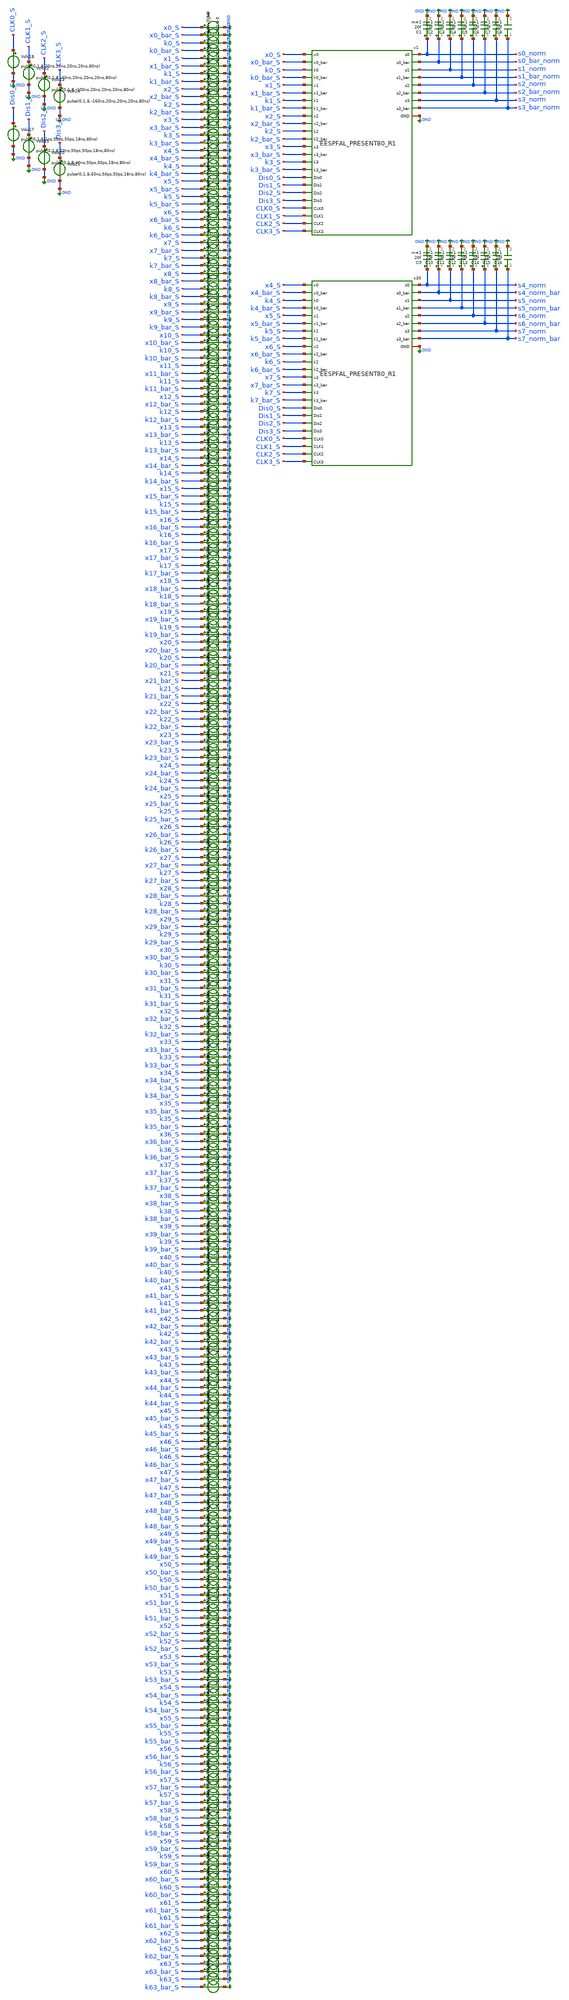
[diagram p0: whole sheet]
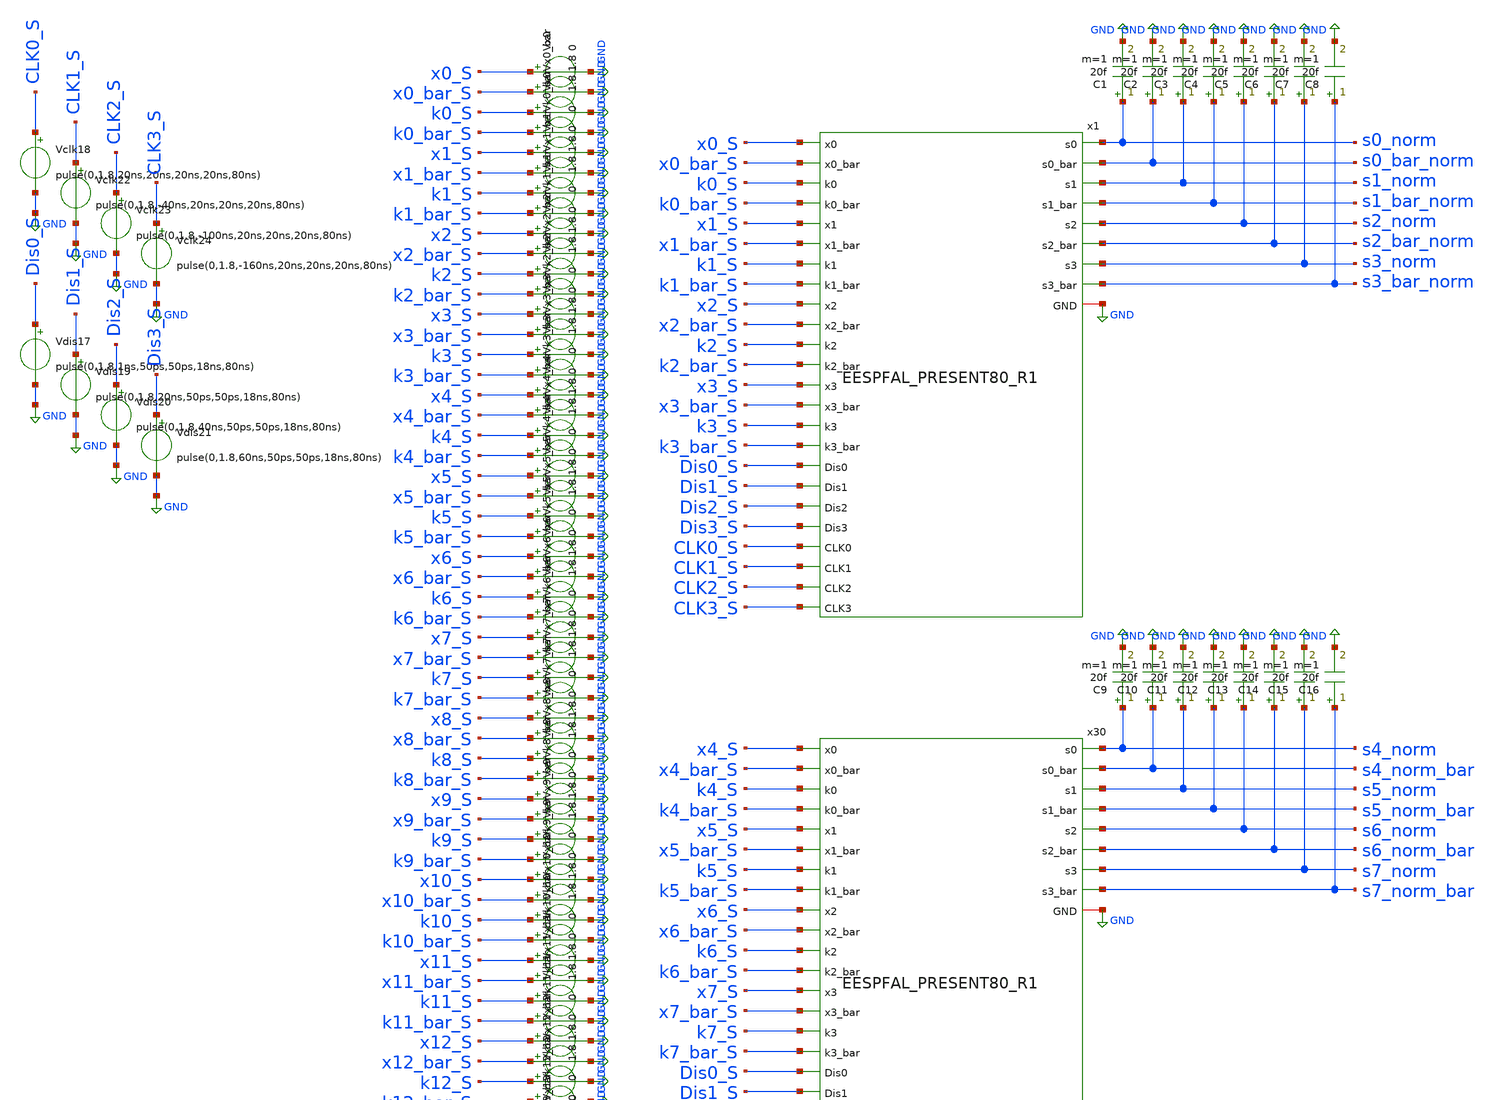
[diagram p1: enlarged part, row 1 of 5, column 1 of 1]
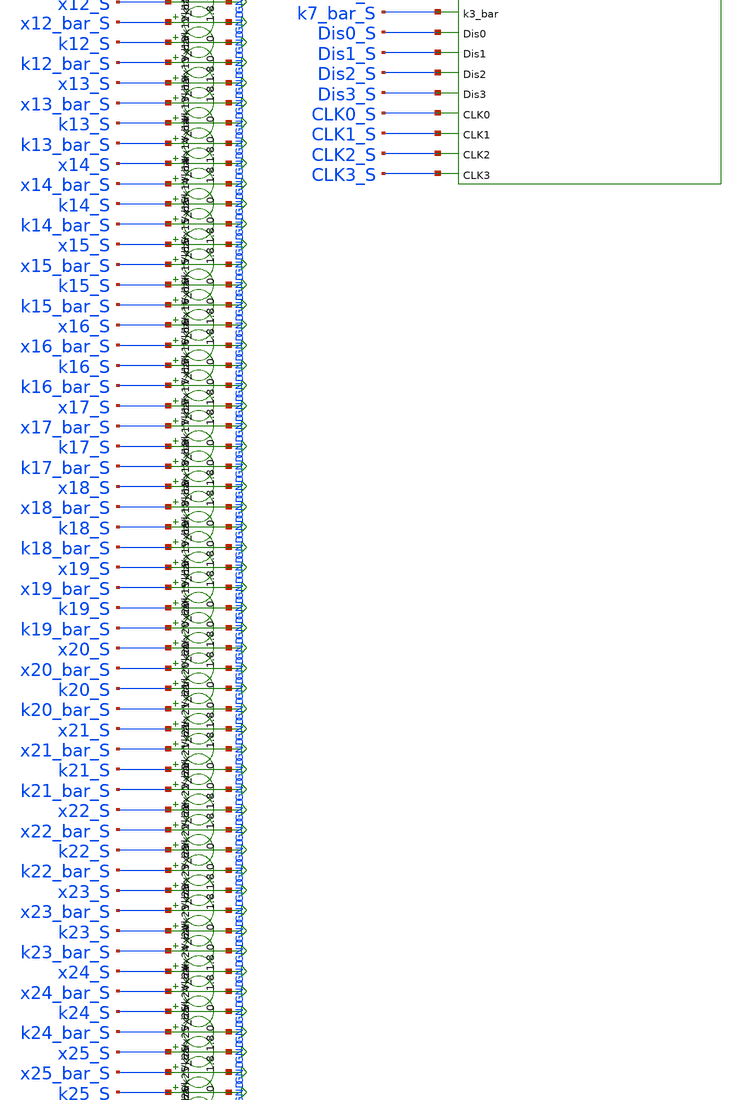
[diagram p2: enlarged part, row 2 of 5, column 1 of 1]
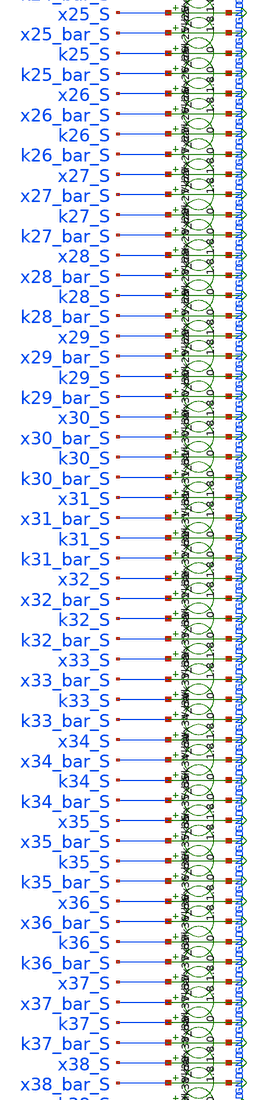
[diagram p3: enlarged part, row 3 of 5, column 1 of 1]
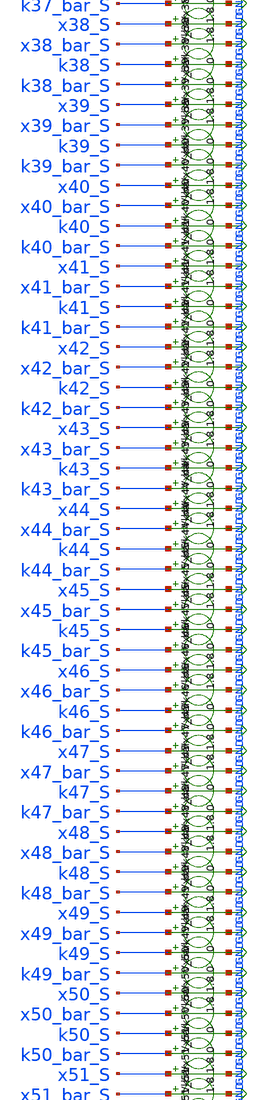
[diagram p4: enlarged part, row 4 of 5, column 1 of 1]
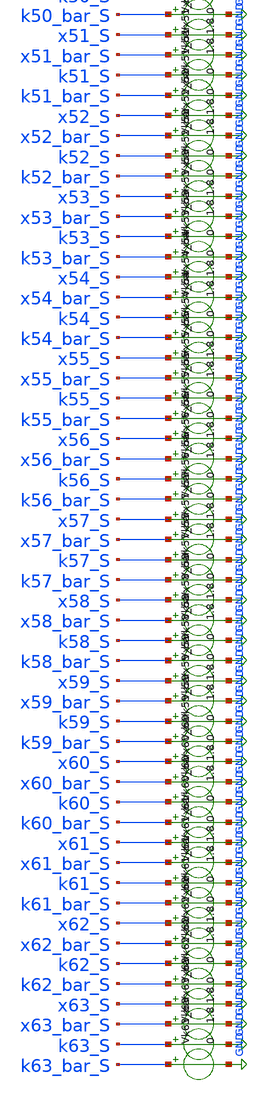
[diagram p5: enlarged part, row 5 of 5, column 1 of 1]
** sch_path: skywater_stuff/EESPFAL_PRESENT80_sim.sch
**.subckt EESPFAL_PRESENT80_sim
Vdis17 Dis0_S GND pulse(0,1.8,1ns,50ps,50ps,18ns,80ns)
Vclk18 CLK0_S GND pulse(0,1.8,20ns,20ns,20ns,20ns,80ns)
Vdis19 Dis1_S GND pulse(0,1.8,20ns,50ps,50ps,18ns,80ns)
Vdis20 Dis2_S GND pulse(0,1.8,40ns,50ps,50ps,18ns,80ns)
Vdis21 Dis3_S GND pulse(0,1.8,60ns,50ps,50ps,18ns,80ns)
Vclk22 CLK1_S GND pulse(0,1.8,-40ns,20ns,20ns,20ns,80ns)
Vclk23 CLK2_S GND pulse(0,1.8,-100ns,20ns,20ns,20ns,80ns)
Vclk24 CLK3_S GND pulse(0,1.8,-160ns,20ns,20ns,20ns,80ns)
C1 s0_norm GND 20f m=1
C2 s0_bar_norm GND 20f m=1
C3 s1_norm GND 20f m=1
C4 s1_bar_norm GND 20f m=1
C5 s2_norm GND 20f m=1
C6 s2_bar_norm GND 20f m=1
C7 s3_norm GND 20f m=1
C8 s3_bar_norm GND 20f m=1
x1 GND x0_S x0_bar_S k0_S k0_bar_S x1_S x1_bar_S k1_S k1_bar_S x2_S x2_bar_S k2_S k2_bar_S x3_S
+ x3_bar_S k3_S k3_bar_S s0_norm s0_bar_norm CLK0_S Dis0_S CLK1_S Dis1_S s2_norm s2_bar_norm s3_bar_norm
+ s3_norm s1_bar_norm s1_norm CLK3_S Dis2_S CLK2_S Dis3_S EESPFAL_PRESENT80_R1
Vx0 x0_S GND 0
Vx0_bar x0_bar_S GND 1.8
Vk0 k0_S GND 1.8
Vk0_bar k0_bar_S GND 0
Vx1 x1_S GND 0
Vx1_bar x1_bar_S GND 1.8
Vk1 k1_S GND 1.8
Vk1_bar k1_bar_S GND 0
Vx2 x2_S GND 0
Vx2_bar x2_bar_S GND 1.8
Vk2 k2_S GND 1.8
Vk2_bar k2_bar_S GND 0
Vx3 x3_S GND 0
Vx3_bar x3_bar_S GND 1.8
Vk3 k3_S GND 1.8
Vk3_bar k3_bar_S GND 0
Vx4 x4_S GND 0
Vx4_bar x4_bar_S GND 1.8
Vk4 k4_S GND 1.8
Vk4_bar k4_bar_S GND 0
Vx5 x5_S GND 0
Vx5_bar x5_bar_S GND 1.8
Vk5 k5_S GND 1.8
Vk5_bar k5_bar_S GND 0
Vx6 x6_S GND 0
Vx6_bar x6_bar_S GND 1.8
Vk6 k6_S GND 1.8
Vk6_bar k6_bar_S GND 0
Vx7 x7_S GND 0
Vx7_bar x7_bar_S GND 1.8
Vk7 k7_S GND 1.8
Vk7_bar k7_bar_S GND 0
Vx8 x8_S GND 0
Vx8_bar x8_bar_S GND 1.8
Vk8 k8_S GND 1.8
Vk8_bar k8_bar_S GND 0
Vx9 x9_S GND 0
Vx9_bar x9_bar_S GND 1.8
Vk9 k9_S GND 1.8
Vk9_bar k9_bar_S GND 0
Vx10 x10_S GND 0
Vx10_bar x10_bar_S GND 1.8
Vk10 k10_S GND 1.8
Vk10_bar k10_bar_S GND 0
Vx11 x11_S GND 0
Vx11_bar x11_bar_S GND 1.8
Vk11 k11_S GND 1.8
Vk11_bar k11_bar_S GND 0
Vx12 x12_S GND 0
Vx12_bar x12_bar_S GND 1.8
Vk12 k12_S GND 1.8
Vk12_bar k12_bar_S GND 0
Vx13 x13_S GND 0
Vx13_bar x13_bar_S GND 1.8
Vk13 k13_S GND 1.8
Vk13_bar k13_bar_S GND 0
Vx14 x14_S GND 0
Vx14_bar x14_bar_S GND 1.8
Vk14 k14_S GND 1.8
Vk14_bar k14_bar_S GND 0
Vx15 x15_S GND 0
Vx15_bar x15_bar_S GND 1.8
Vk15 k15_S GND 1.8
Vk15_bar k15_bar_S GND 0
Vx16 x16_S GND 0
Vx16_bar x16_bar_S GND 1.8
Vk16 k16_S GND 1.8
Vk16_bar k16_bar_S GND 0
Vx17 x17_S GND 0
Vx17_bar x17_bar_S GND 1.8
Vk17 k17_S GND 1.8
Vk17_bar k17_bar_S GND 0
Vx18 x18_S GND 0
Vx18_bar x18_bar_S GND 1.8
Vk18 k18_S GND 1.8
Vk18_bar k18_bar_S GND 0
Vx19 x19_S GND 0
Vx19_bar x19_bar_S GND 1.8
Vk19 k19_S GND 1.8
Vk19_bar k19_bar_S GND 0
Vx20 x20_S GND 0
Vx20_bar x20_bar_S GND 1.8
Vk20 k20_S GND 1.8
Vk20_bar k20_bar_S GND 0
Vx21 x21_S GND 0
Vx21_bar x21_bar_S GND 1.8
Vk21 k21_S GND 1.8
Vk21_bar k21_bar_S GND 0
Vx22 x22_S GND 0
Vx22_bar x22_bar_S GND 1.8
Vk22 k22_S GND 1.8
Vk22_bar k22_bar_S GND 0
Vx23 x23_S GND 0
Vx23_bar x23_bar_S GND 1.8
Vk23 k23_S GND 1.8
Vk23_bar k23_bar_S GND 0
Vx24 x24_S GND 0
Vx24_bar x24_bar_S GND 1.8
Vk24 k24_S GND 1.8
Vk24_bar k24_bar_S GND 0
Vx25 x25_S GND 0
Vx25_bar x25_bar_S GND 1.8
Vk25 k25_S GND 1.8
Vk25_bar k25_bar_S GND 0
Vx26 x26_S GND 0
Vx26_bar x26_bar_S GND 1.8
Vk26 k26_S GND 1.8
Vk26_bar k26_bar_S GND 0
Vx27 x27_S GND 0
Vx27_bar x27_bar_S GND 1.8
Vk27 k27_S GND 1.8
Vk27_bar k27_bar_S GND 0
Vx28 x28_S GND 0
Vx28_bar x28_bar_S GND 1.8
Vk28 k28_S GND 1.8
Vk28_bar k28_bar_S GND 0
Vx29 x29_S GND 0
Vx29_bar x29_bar_S GND 1.8
Vk29 k29_S GND 1.8
Vk29_bar k29_bar_S GND 0
Vx30 x30_S GND 0
Vx30_bar x30_bar_S GND 1.8
Vk30 k30_S GND 1.8
Vk30_bar k30_bar_S GND 0
Vx31 x31_S GND 0
Vx31_bar x31_bar_S GND 1.8
Vk31 k31_S GND 1.8
Vk31_bar k31_bar_S GND 0
Vx32 x32_S GND 0
Vx32_bar x32_bar_S GND 1.8
Vk32 k32_S GND 1.8
Vk32_bar k32_bar_S GND 0
Vx33 x33_S GND 0
Vx33_bar x33_bar_S GND 1.8
Vk33 k33_S GND 1.8
Vk33_bar k33_bar_S GND 0
Vx34 x34_S GND 0
Vx34_bar x34_bar_S GND 1.8
Vk34 k34_S GND 1.8
Vk34_bar k34_bar_S GND 0
Vx35 x35_S GND 0
Vx35_bar x35_bar_S GND 1.8
Vk35 k35_S GND 1.8
Vk35_bar k35_bar_S GND 0
Vx36 x36_S GND 0
Vx36_bar x36_bar_S GND 1.8
Vk36 k36_S GND 1.8
Vk36_bar k36_bar_S GND 0
Vx37 x37_S GND 0
Vx37_bar x37_bar_S GND 1.8
Vk37 k37_S GND 1.8
Vk37_bar k37_bar_S GND 0
Vx38 x38_S GND 0
Vx38_bar x38_bar_S GND 1.8
Vk38 k38_S GND 1.8
Vk38_bar k38_bar_S GND 0
Vx39 x39_S GND 0
Vx39_bar x39_bar_S GND 1.8
Vk39 k39_S GND 1.8
Vk39_bar k39_bar_S GND 0
Vx40 x40_S GND 0
Vx40_bar x40_bar_S GND 1.8
Vk40 k40_S GND 1.8
Vk40_bar k40_bar_S GND 0
Vx41 x41_S GND 0
Vx41_bar x41_bar_S GND 1.8
Vk41 k41_S GND 1.8
Vk41_bar k41_bar_S GND 0
Vx42 x42_S GND 0
Vx42_bar x42_bar_S GND 1.8
Vk42 k42_S GND 1.8
Vk42_bar k42_bar_S GND 0
Vx43 x43_S GND 0
Vx43_bar x43_bar_S GND 1.8
Vk43 k43_S GND 1.8
Vk43_bar k43_bar_S GND 0
Vx44 x44_S GND 0
Vx44_bar x44_bar_S GND 1.8
Vk44 k44_S GND 1.8
Vk44_bar k44_bar_S GND 0
Vx45 x45_S GND 0
Vx45_bar x45_bar_S GND 1.8
Vk45 k45_S GND 1.8
Vk45_bar k45_bar_S GND 0
Vx46 x46_S GND 0
Vx46_bar x46_bar_S GND 1.8
Vk46 k46_S GND 1.8
Vk46_bar k46_bar_S GND 0
Vx47 x47_S GND 0
Vx47_bar x47_bar_S GND 1.8
Vk47 k47_S GND 1.8
Vk47_bar k47_bar_S GND 0
Vx48 x48_S GND 0
Vx48_bar x48_bar_S GND 1.8
Vk48 k48_S GND 1.8
Vk48_bar k48_bar_S GND 0
Vx49 x49_S GND 0
Vx49_bar x49_bar_S GND 1.8
Vk49 k49_S GND 1.8
Vk49_bar k49_bar_S GND 0
Vx50 x50_S GND 0
Vx50_bar x50_bar_S GND 1.8
Vk50 k50_S GND 1.8
Vk50_bar k50_bar_S GND 0
Vx51 x51_S GND 0
Vx51_bar x51_bar_S GND 1.8
Vk51 k51_S GND 1.8
Vk51_bar k51_bar_S GND 0
Vx52 x52_S GND 0
Vx52_bar x52_bar_S GND 1.8
Vk52 k52_S GND 1.8
Vk52_bar k52_bar_S GND 0
Vx53 x53_S GND 0
Vx53_bar x53_bar_S GND 1.8
Vk53 k53_S GND 1.8
Vk53_bar k53_bar_S GND 0
Vx54 x54_S GND 0
Vx54_bar x54_bar_S GND 1.8
Vk54 k54_S GND 1.8
Vk54_bar k54_bar_S GND 0
Vx55 x55_S GND 0
Vx55_bar x55_bar_S GND 1.8
Vk55 k55_S GND 1.8
Vk55_bar k55_bar_S GND 0
Vx56 x56_S GND 0
Vx56_bar x56_bar_S GND 1.8
Vk56 k56_S GND 1.8
Vk56_bar k56_bar_S GND 0
Vx57 x57_S GND 0
Vx57_bar x57_bar_S GND 1.8
Vk57 k57_S GND 1.8
Vk57_bar k57_bar_S GND 0
Vx58 x58_S GND 0
Vx58_bar x58_bar_S GND 1.8
Vk58 k58_S GND 1.8
Vk58_bar k58_bar_S GND 0
Vx59 x59_S GND 0
Vx59_bar x59_bar_S GND 1.8
Vk59 k59_S GND 1.8
Vk59_bar k59_bar_S GND 0
Vx60 x60_S GND 0
Vx60_bar x60_bar_S GND 1.8
Vk60 k60_S GND 1.8
Vk60_bar k60_bar_S GND 0
Vx61 x61_S GND 0
Vx61_bar x61_bar_S GND 1.8
Vk61 k61_S GND 1.8
Vk61_bar k61_bar_S GND 0
Vx62 x62_S GND 0
Vx62_bar x62_bar_S GND 1.8
Vk62 k62_S GND 1.8
Vk62_bar k62_bar_S GND 0
Vx63 x63_S GND 0
Vx63_bar x63_bar_S GND 1.8
Vk63 k63_S GND 1.8
Vk63_bar k63_bar_S GND 0
x30 GND x4_S x4_bar_S k4_S k4_bar_S x5_S x5_bar_S k5_S k5_bar_S x6_S x6_bar_S k6_S k6_bar_S x7_S
+ x7_bar_S k7_S k7_bar_S s4_norm s4_norm_bar CLK0_S Dis0_S CLK1_S Dis1_S s6_norm s6_norm_bar s7_norm_bar
+ s7_norm s5_norm_bar s5_norm CLK3_S Dis2_S CLK2_S Dis3_S EESPFAL_PRESENT80_R1
C9 s4_norm GND 20f m=1
C10 s4_norm_bar GND 20f m=1
C11 s5_norm GND 20f m=1
C12 s5_norm_bar GND 20f m=1
C13 s6_norm GND 20f m=1
C14 s6_norm_bar GND 20f m=1
C15 s7_norm GND 20f m=1
C16 s7_norm_bar GND 20f m=1
**** begin user architecture code

.lib /research/pdk/open_pdks/share/pdk/sky130A/libs.tech/ngspice/sky130.lib.spice tt
**.include ~/magic_layout_stuff/EESPFAL_PRESENT80_R1.spice
**.include ~/magic_layout_stuff/EESPFAL_PRESENT80_R1_flat.spice
.param v0 ='0' v0_bar ='1.8' v1 ='0' v1_bar ='1.8' v2 ='0' v2_bar ='1.8' v3 ='0' v3_bar ='1.8'
.option method=gear
.control
echo We at start now
set tstart=0
*set tstop=0
let index=0
let index2=1
let wstart = $tstart
let wstop = 0n
let key = 7
let total_time = 5
let cycle_index = 1

*foreach bit_index 0 1 2 3
*	set bit = `./test.sh $&key $bit_index`
*	alter Vk$bit_index = '$bit ? 1.8 : 0'
*	alter Vk`echo $bit_index`_bar = '$bit ? 0 : 1.8'
*end

let bit_index = 0
while bit_index < 8
	set bit = `./test.sh $&key $&bit_index`
	alter Vk$&bit_index = '$bit ? 1.8 : 0'
	alter Vk`echo $&bit_index`_bar = '$bit ? 0 : 1.8'
	let bit_index = bit_index + 1
end

*set values_raw < circ_inputs_`echo $&cycle_index`.txt
set values_raw < circ_inputs_not_rand_`echo $&cycle_index`.txt
compose values values $values_raw
echo stuff

*let curr_time = index*80n

while index2 < length(values)
	let wstop = $&index2*80n
	stop when time=$&wstop
	let index2 = $&index2+1
	echo $&index2
end

let tstop = length(values)*80n
while index < length(values)
	let value = values[$&index]
	echo $&value
	echo going into altering
	let bit_index = 0
	while bit_index < 8
		set bit = `./test.sh $&value $&bit_index`
		alter Vx$&bit_index = '$bit ? 1.8 : 0'
		alter Vx`echo $&bit_index`_bar = '$bit ? 0 : 1.8'
		let bit_index = bit_index + 1
	end
	echo test stuff
	let index=index+1
	if index = 1
		tran 1n $&tstop 0 1n
	else
		resume
	end
end

*let Pinst_CLK0_CLK3 =
*+ (v(CLK0_S)*i(vclk18))+(v(CLK1_S)*i(vclk22))+(v(CLK2_S)*i(vclk23))+(v(CLK3_S)*i(vclk24))
*plot Pinst_CLK0_CLK3
let index = 0
while index < length(values)
	let Pinst_CLK0_CLK3 =
+ (v(CLK0_S)*i(vclk18))+(v(CLK1_S)*i(vclk22))+(v(CLK2_S)*i(vclk23))+(v(CLK3_S)*i(vclk24))
	**let Pinst_CLK0_CLK3_Dis0_Dis3 =
+ (v(CLK0_S)*i(vclk18))+(v(CLK1_S)*i(vclk22))+(v(CLK2_S)*i(vclk23))+(v(CLK3_S)*i(vclk24))+(v(Dis0_S)*i(vdis17))+(v(Dis1_S)*i(vdis19))+(v(Dis2_S)*i(vdis20))+(v(Dis3_S)*i(vdis21))
	**plot Pinst_CLK0_CLK3
	let lin-tstart = $&index*80ns
	let lin-tstop = $&lin-tstart+80ns
	let lin-tstep = 0.1n
	linearize Pinst_CLK0_CLK3
	*display
	set appendwrite
	*wrdata EESPFAL_K`echo $&key`_`echo $&total_time`u_`echo $&cycle_index`cycle_norm.csv
+ Pinst_CLK0_CLK3
	*wrdata EESPFAL_FULL_R1_K`echo $&key`_`echo $&total_time`u_`echo $&cycle_index`cycle_norm.csv
+ Pinst_CLK0_CLK3
	*wrdata EESPFAL_32bits_K`echo $&key`_`echo $&total_time`u_`echo $&cycle_index`cycle_norm.csv
+ Pinst_CLK0_CLK3
	*wrdata EESPFAL_K`echo $&key`_`echo $&total_time`u_`echo $&cycle_index`cycle_flat.csv
+ Pinst_CLK0_CLK3
	let index = index + 1
	*echo $plots
	setplot tran1
	destroy tran2
	*echo $plots
end
	plot v(CLK0_S)
	plot v(CLK3_S)
	plot v(s0_norm)
	plot v(s2_norm)
	plot v(s4_norm)
	plot v(s6_norm)
.endc


**** end user architecture code
**.ends
.GLOBAL GND
.end
